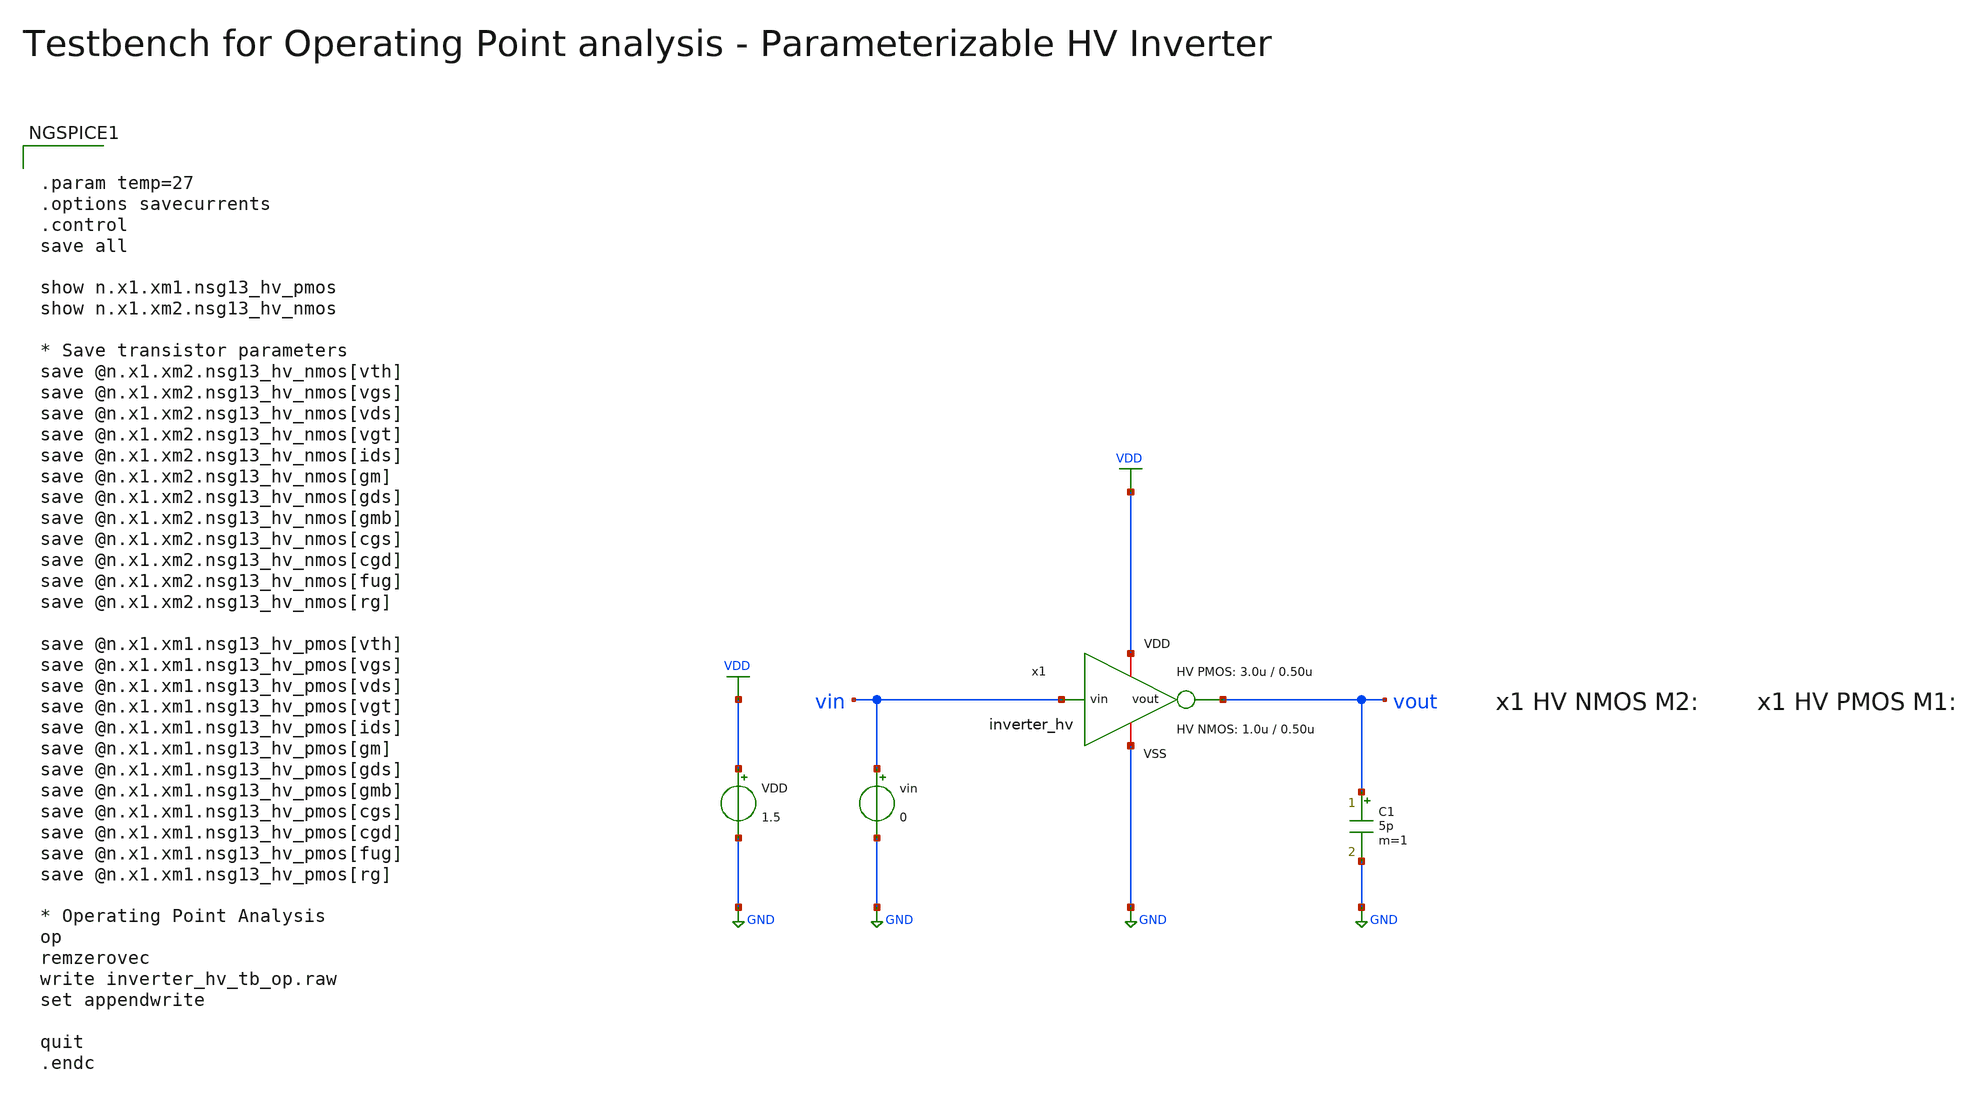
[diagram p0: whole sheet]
** sch_path: SG13G2_ATBS-ADC-main/xschem/inverter/testbenches/inverter_hv_tb_op.sch
**.subckt inverter_hv_tb_op
VDD VDD GND 1.5
C1 vout GND 5p m=1
vin vin GND 0
x1 VDD vin vout GND inverter_hv W_P=3.0u L_P=0.50u W_N=1.0u L_N=0.50u
**** begin user architecture code

.lib cornerMOShv.lib mos_tt
.lib cornerRES.lib res_typ



.param temp=27
.options savecurrents
.control
save all

show n.x1.xm1.nsg13_hv_pmos
show n.x1.xm2.nsg13_hv_nmos

* Save transistor parameters
save @n.x1.xm2.nsg13_hv_nmos[vth]
save @n.x1.xm2.nsg13_hv_nmos[vgs]
save @n.x1.xm2.nsg13_hv_nmos[vds]
save @n.x1.xm2.nsg13_hv_nmos[vgt]
save @n.x1.xm2.nsg13_hv_nmos[ids]
save @n.x1.xm2.nsg13_hv_nmos[gm]
save @n.x1.xm2.nsg13_hv_nmos[gds]
save @n.x1.xm2.nsg13_hv_nmos[gmb]
save @n.x1.xm2.nsg13_hv_nmos[cgs]
save @n.x1.xm2.nsg13_hv_nmos[cgd]
save @n.x1.xm2.nsg13_hv_nmos[fug]
save @n.x1.xm2.nsg13_hv_nmos[rg]

save @n.x1.xm1.nsg13_hv_pmos[vth]
save @n.x1.xm1.nsg13_hv_pmos[vgs]
save @n.x1.xm1.nsg13_hv_pmos[vds]
save @n.x1.xm1.nsg13_hv_pmos[vgt]
save @n.x1.xm1.nsg13_hv_pmos[ids]
save @n.x1.xm1.nsg13_hv_pmos[gm]
save @n.x1.xm1.nsg13_hv_pmos[gds]
save @n.x1.xm1.nsg13_hv_pmos[gmb]
save @n.x1.xm1.nsg13_hv_pmos[cgs]
save @n.x1.xm1.nsg13_hv_pmos[cgd]
save @n.x1.xm1.nsg13_hv_pmos[fug]
save @n.x1.xm1.nsg13_hv_pmos[rg]

* Operating Point Analysis
op
remzerovec
write inverter_hv_tb_op.raw
set appendwrite

quit
.endc

**** end user architecture code
**.ends

* expanding   symbol:  inverter/inverter_hv.sym # of pins=4
** sym_path: SG13G2_ATBS-ADC-main/xschem/inverter/inverter_hv.sym
** sch_path: SG13G2_ATBS-ADC-main/xschem/inverter/inverter_hv.sch
.subckt inverter_hv VDD vin vout VSS  W_P=3.0u L_P=0.50u W_N=1.0u L_N=0.50u
*.ipin vin
*.iopin VDD
*.iopin VSS
*.opin vout
XM1 vout vin VDD VDD sg13_hv_pmos w=W_P l=L_P ng=1 m=1 mm_ok=1
XM2 vout vin VSS VSS sg13_hv_nmos w=W_N l=L_N ng=1 m=1 mm_ok=1
.ends

.GLOBAL GND
.GLOBAL VDD
.end
